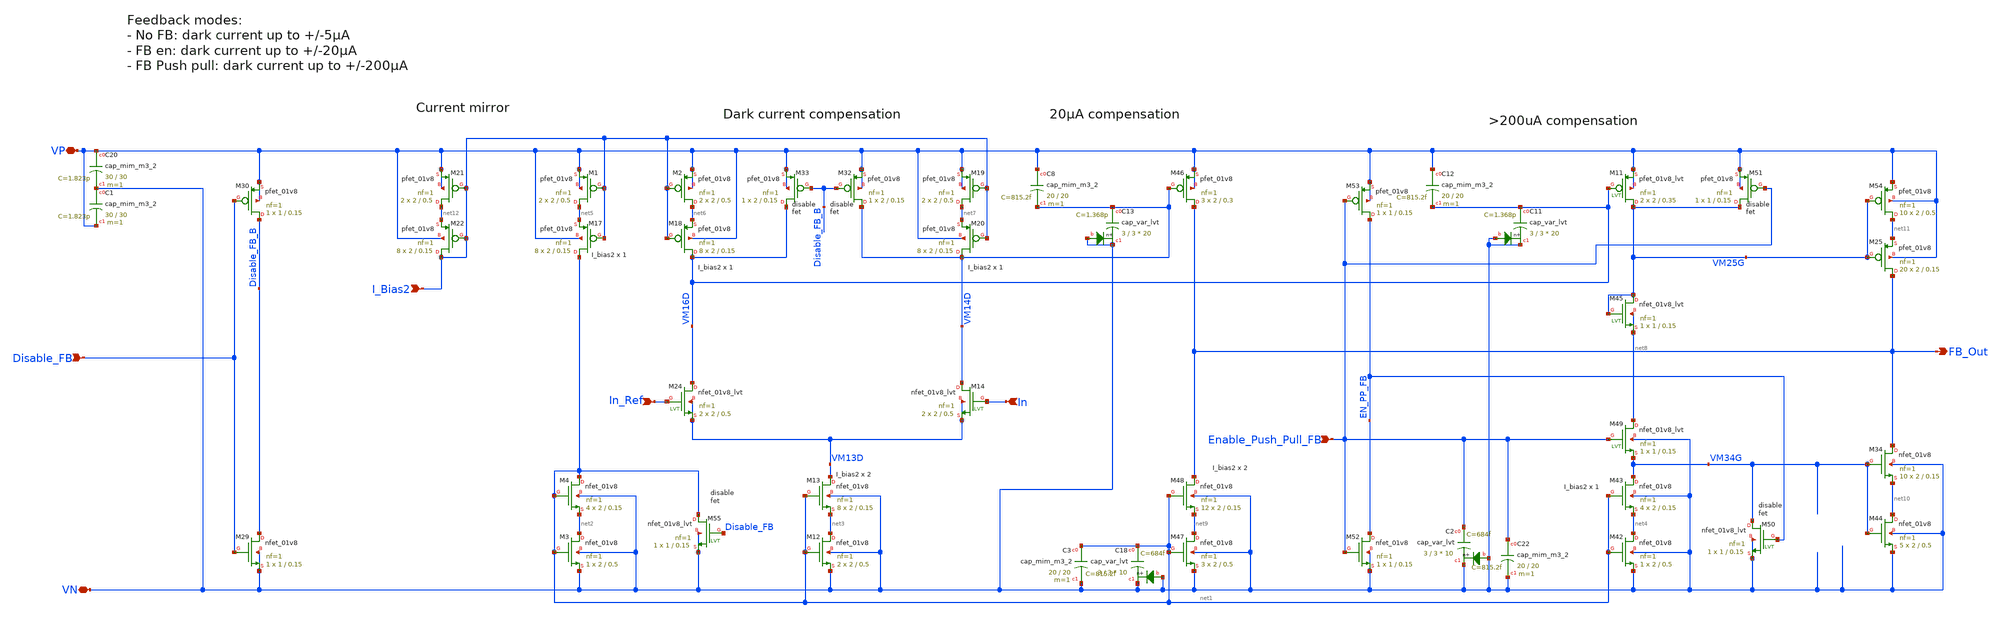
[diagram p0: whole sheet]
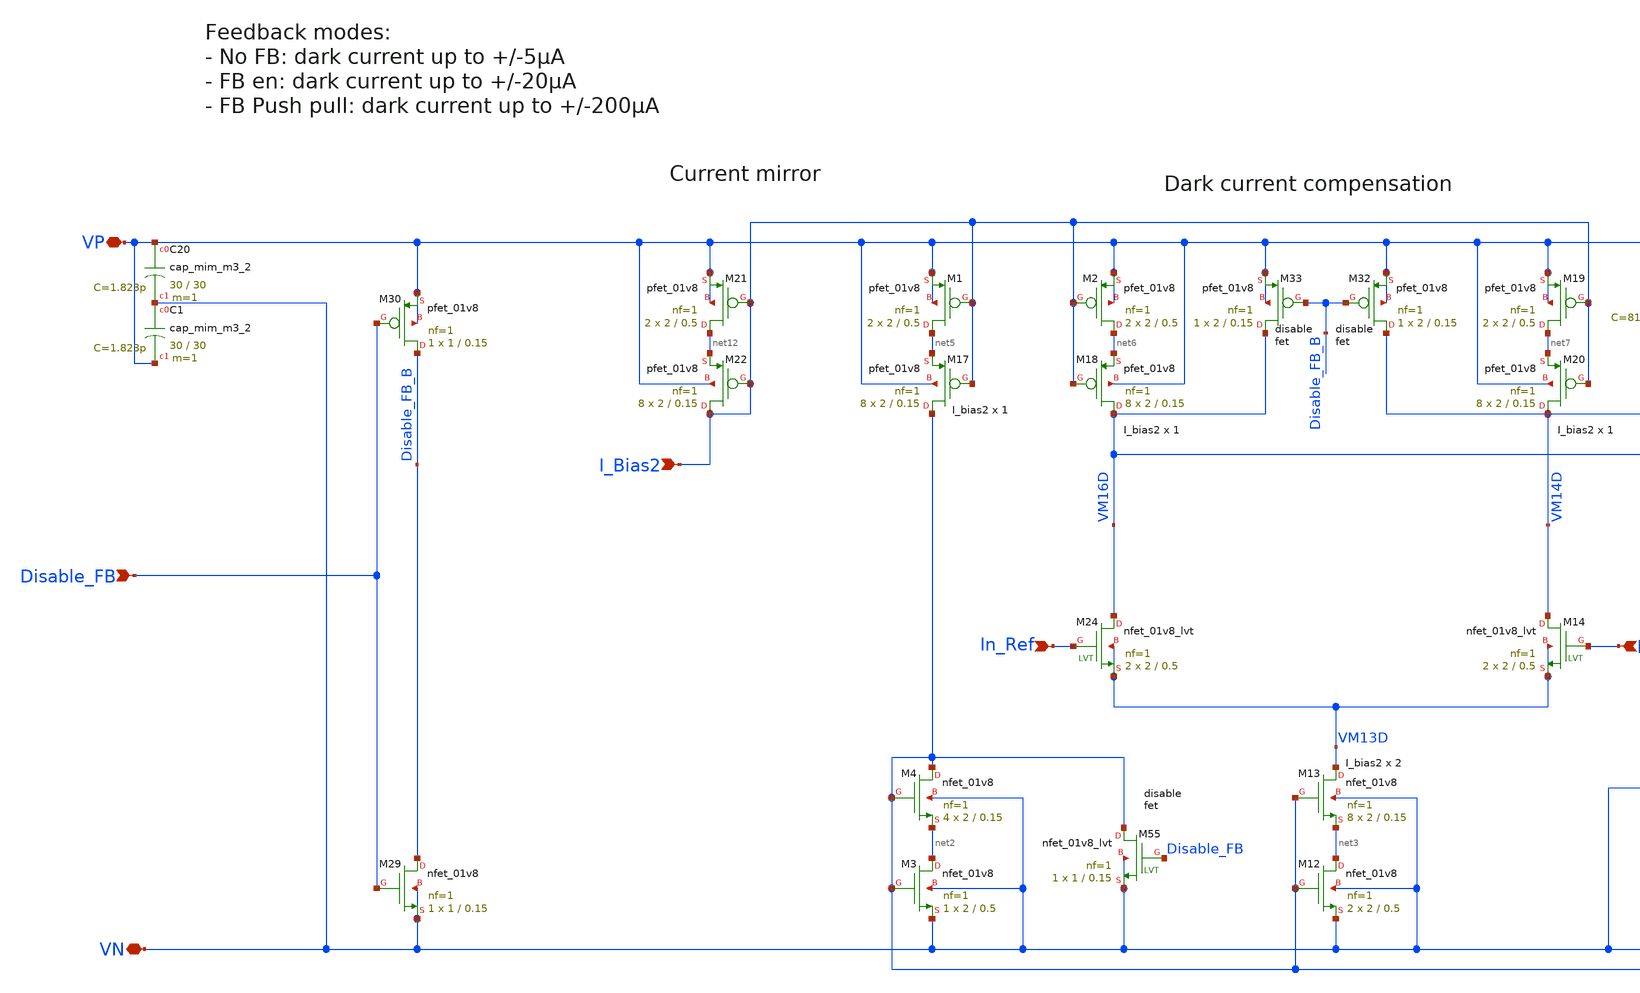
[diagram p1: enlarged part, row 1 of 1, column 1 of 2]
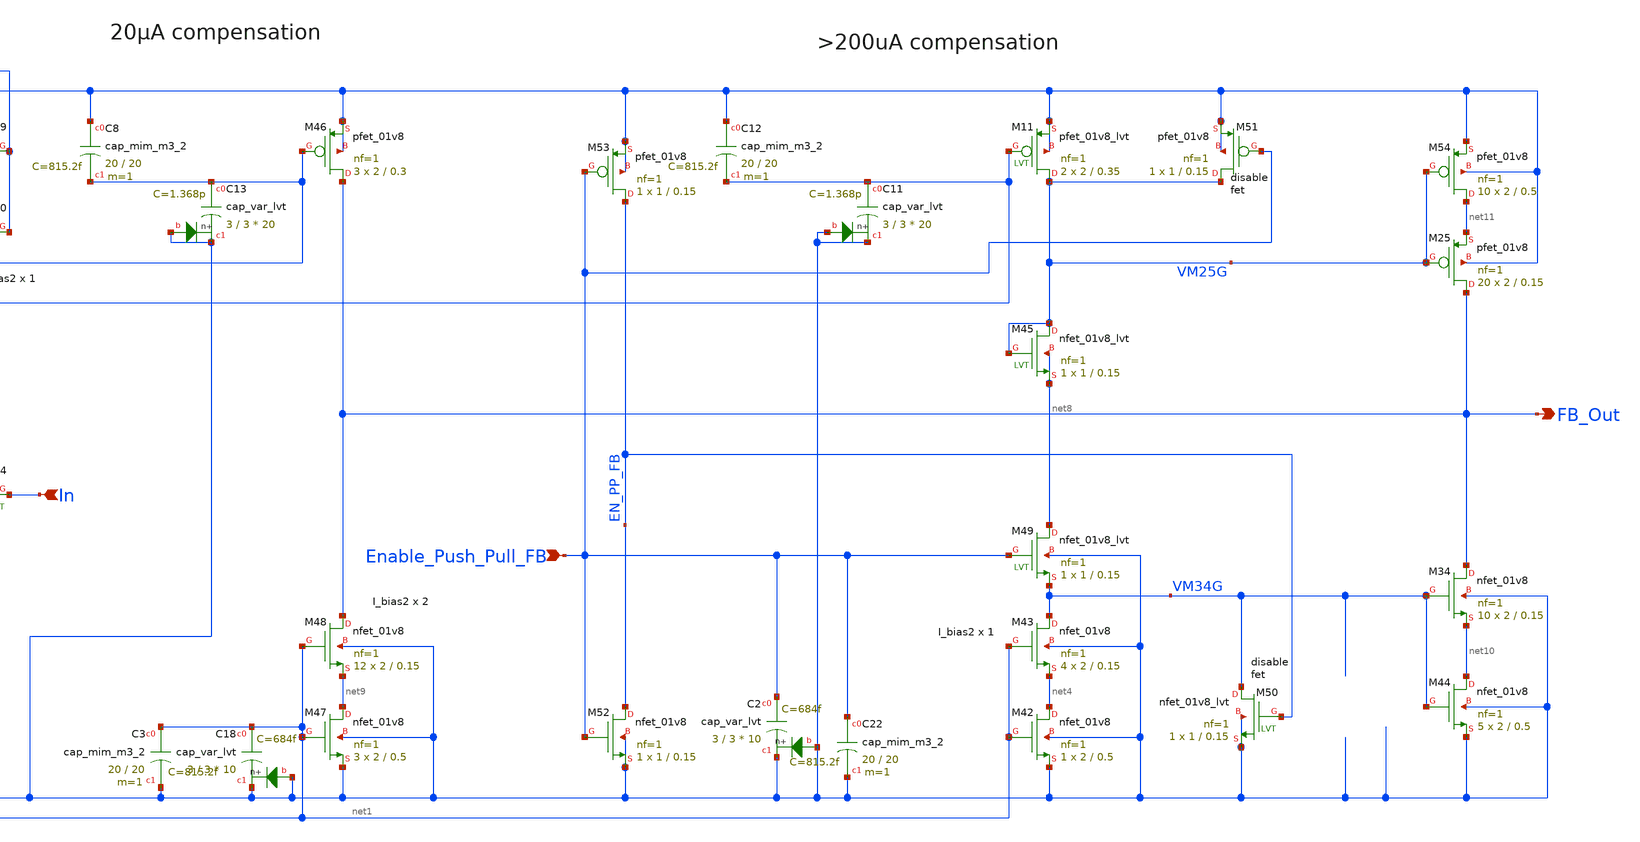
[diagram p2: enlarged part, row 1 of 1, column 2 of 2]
** sch_path: xschem/tia/tia_rgc_feedback.sch
**.subckt tia_rgc_feedback VN VP I_Bias2 Disable_FB Enable_Push_Pull_FB In_Ref FB_Out In
*.iopin VN
*.iopin VP
*.ipin I_Bias2
*.ipin Disable_FB
*.ipin Enable_Push_Pull_FB
*.ipin In_Ref
*.opin FB_Out
*.ipin In
XM3 net2 net1 VN VN sky130_fd_pr__nfet_01v8 L=0.5 W=2 nf=1 ad='int((nf+1)/2) * W/nf * 0.29' as='int((nf+2)/2) * W/nf * 0.29'
+ pd='2*int((nf+1)/2) * (W/nf + 0.29)' ps='2*int((nf+2)/2) * (W/nf + 0.29)' nrd='0.29 / W' nrs='0.29 / W'
+ sa=0 sb=0 sd=0 mult=1 m=1
XM4 net1 net1 net2 VN sky130_fd_pr__nfet_01v8 L=0.15 W=2 nf=1 ad='int((nf+1)/2) * W/nf * 0.29' as='int((nf+2)/2) * W/nf * 0.29'
+ pd='2*int((nf+1)/2) * (W/nf + 0.29)' ps='2*int((nf+2)/2) * (W/nf + 0.29)' nrd='0.29 / W' nrs='0.29 / W'
+ sa=0 sb=0 sd=0 mult=4 m=4
XM12 net3 net1 VN VN sky130_fd_pr__nfet_01v8 L=0.5 W=2 nf=1 ad='int((nf+1)/2) * W/nf * 0.29' as='int((nf+2)/2) * W/nf * 0.29'
+ pd='2*int((nf+1)/2) * (W/nf + 0.29)' ps='2*int((nf+2)/2) * (W/nf + 0.29)' nrd='0.29 / W' nrs='0.29 / W'
+ sa=0 sb=0 sd=0 mult=2 m=2
XM13 VM13D net1 net3 VN sky130_fd_pr__nfet_01v8 L=0.15 W=2 nf=1 ad='int((nf+1)/2) * W/nf * 0.29' as='int((nf+2)/2) * W/nf * 0.29'
+ pd='2*int((nf+1)/2) * (W/nf + 0.29)' ps='2*int((nf+2)/2) * (W/nf + 0.29)' nrd='0.29 / W' nrs='0.29 / W'
+ sa=0 sb=0 sd=0 mult=8 m=8
XM1 net5 I_Bias2 VP VP sky130_fd_pr__pfet_01v8 L=0.5 W=2 nf=1 ad='int((nf+1)/2) * W/nf * 0.29' as='int((nf+2)/2) * W/nf * 0.29'
+ pd='2*int((nf+1)/2) * (W/nf + 0.29)' ps='2*int((nf+2)/2) * (W/nf + 0.29)' nrd='0.29 / W' nrs='0.29 / W'
+ sa=0 sb=0 sd=0 mult=2 m=2
XM29 Disable_FB_B Disable_FB VN VN sky130_fd_pr__nfet_01v8 L=0.15 W=1 nf=1 ad='int((nf+1)/2) * W/nf * 0.29'
+ as='int((nf+2)/2) * W/nf * 0.29' pd='2*int((nf+1)/2) * (W/nf + 0.29)' ps='2*int((nf+2)/2) * (W/nf + 0.29)'
+ nrd='0.29 / W' nrs='0.29 / W' sa=0 sb=0 sd=0 mult=1 m=1
XM30 Disable_FB_B Disable_FB VP VP sky130_fd_pr__pfet_01v8 L=0.15 W=1 nf=1 ad='int((nf+1)/2) * W/nf * 0.29'
+ as='int((nf+2)/2) * W/nf * 0.29' pd='2*int((nf+1)/2) * (W/nf + 0.29)' ps='2*int((nf+2)/2) * (W/nf + 0.29)'
+ nrd='0.29 / W' nrs='0.29 / W' sa=0 sb=0 sd=0 mult=1 m=1
XM32 VM14D Disable_FB_B VP VP sky130_fd_pr__pfet_01v8 L=0.15 W=2 nf=1 ad='int((nf+1)/2) * W/nf * 0.29'
+ as='int((nf+2)/2) * W/nf * 0.29' pd='2*int((nf+1)/2) * (W/nf + 0.29)' ps='2*int((nf+2)/2) * (W/nf + 0.29)'
+ nrd='0.29 / W' nrs='0.29 / W' sa=0 sb=0 sd=0 mult=1 m=1
XM33 VM16D Disable_FB_B VP VP sky130_fd_pr__pfet_01v8 L=0.15 W=2 nf=1 ad='int((nf+1)/2) * W/nf * 0.29'
+ as='int((nf+2)/2) * W/nf * 0.29' pd='2*int((nf+1)/2) * (W/nf + 0.29)' ps='2*int((nf+2)/2) * (W/nf + 0.29)'
+ nrd='0.29 / W' nrs='0.29 / W' sa=0 sb=0 sd=0 mult=1 m=1
XM42 net4 net1 VN VN sky130_fd_pr__nfet_01v8 L=0.5 W=2 nf=1 ad='int((nf+1)/2) * W/nf * 0.29' as='int((nf+2)/2) * W/nf * 0.29'
+ pd='2*int((nf+1)/2) * (W/nf + 0.29)' ps='2*int((nf+2)/2) * (W/nf + 0.29)' nrd='0.29 / W' nrs='0.29 / W'
+ sa=0 sb=0 sd=0 mult=1 m=1
XM43 VM34G net1 net4 VN sky130_fd_pr__nfet_01v8 L=0.15 W=2 nf=1 ad='int((nf+1)/2) * W/nf * 0.29' as='int((nf+2)/2) * W/nf * 0.29'
+ pd='2*int((nf+1)/2) * (W/nf + 0.29)' ps='2*int((nf+2)/2) * (W/nf + 0.29)' nrd='0.29 / W' nrs='0.29 / W'
+ sa=0 sb=0 sd=0 mult=4 m=4
XM17 net1 I_Bias2 net5 VP sky130_fd_pr__pfet_01v8 L=0.15 W=2 nf=1 ad='int((nf+1)/2) * W/nf * 0.29' as='int((nf+2)/2) * W/nf * 0.29'
+ pd='2*int((nf+1)/2) * (W/nf + 0.29)' ps='2*int((nf+2)/2) * (W/nf + 0.29)' nrd='0.29 / W' nrs='0.29 / W'
+ sa=0 sb=0 sd=0 mult=8 m=8
XM2 net6 I_Bias2 VP VP sky130_fd_pr__pfet_01v8 L=0.5 W=2 nf=1 ad='int((nf+1)/2) * W/nf * 0.29' as='int((nf+2)/2) * W/nf * 0.29'
+ pd='2*int((nf+1)/2) * (W/nf + 0.29)' ps='2*int((nf+2)/2) * (W/nf + 0.29)' nrd='0.29 / W' nrs='0.29 / W'
+ sa=0 sb=0 sd=0 mult=2 m=2
XM18 VM16D I_Bias2 net6 VP sky130_fd_pr__pfet_01v8 L=0.15 W=2 nf=1 ad='int((nf+1)/2) * W/nf * 0.29' as='int((nf+2)/2) * W/nf * 0.29'
+ pd='2*int((nf+1)/2) * (W/nf + 0.29)' ps='2*int((nf+2)/2) * (W/nf + 0.29)' nrd='0.29 / W' nrs='0.29 / W'
+ sa=0 sb=0 sd=0 mult=8 m=8
XM19 net7 I_Bias2 VP VP sky130_fd_pr__pfet_01v8 L=0.5 W=2 nf=1 ad='int((nf+1)/2) * W/nf * 0.29' as='int((nf+2)/2) * W/nf * 0.29'
+ pd='2*int((nf+1)/2) * (W/nf + 0.29)' ps='2*int((nf+2)/2) * (W/nf + 0.29)' nrd='0.29 / W' nrs='0.29 / W'
+ sa=0 sb=0 sd=0 mult=2 m=2
XM20 VM14D I_Bias2 net7 VP sky130_fd_pr__pfet_01v8 L=0.15 W=2 nf=1 ad='int((nf+1)/2) * W/nf * 0.29' as='int((nf+2)/2) * W/nf * 0.29'
+ pd='2*int((nf+1)/2) * (W/nf + 0.29)' ps='2*int((nf+2)/2) * (W/nf + 0.29)' nrd='0.29 / W' nrs='0.29 / W'
+ sa=0 sb=0 sd=0 mult=8 m=8
XM34 FB_Out VM34G net10 VN sky130_fd_pr__nfet_01v8 L=0.15 W=2 nf=1 ad='int((nf+1)/2) * W/nf * 0.29' as='int((nf+2)/2) * W/nf * 0.29'
+ pd='2*int((nf+1)/2) * (W/nf + 0.29)' ps='2*int((nf+2)/2) * (W/nf + 0.29)' nrd='0.29 / W' nrs='0.29 / W'
+ sa=0 sb=0 sd=0 mult=10 m=10
XM25 FB_Out VM25G net11 VP sky130_fd_pr__pfet_01v8 L=0.15 W=2 nf=1 ad='int((nf+1)/2) * W/nf * 0.29' as='int((nf+2)/2) * W/nf * 0.29'
+ pd='2*int((nf+1)/2) * (W/nf + 0.29)' ps='2*int((nf+2)/2) * (W/nf + 0.29)' nrd='0.29 / W' nrs='0.29 / W'
+ sa=0 sb=0 sd=0 mult=20 m=20
XM45 VM25G VM25G net8 net8 sky130_fd_pr__nfet_01v8_lvt L=0.15 W=1 nf=1 ad='int((nf+1)/2) * W/nf * 0.29'
+ as='int((nf+2)/2) * W/nf * 0.29' pd='2*int((nf+1)/2) * (W/nf + 0.29)' ps='2*int((nf+2)/2) * (W/nf + 0.29)'
+ nrd='0.29 / W' nrs='0.29 / W' sa=0 sb=0 sd=0 mult=1 m=1
XM46 FB_Out VM14D VP VP sky130_fd_pr__pfet_01v8 L=0.3 W=2 nf=1 ad='int((nf+1)/2) * W/nf * 0.29' as='int((nf+2)/2) * W/nf * 0.29'
+ pd='2*int((nf+1)/2) * (W/nf + 0.29)' ps='2*int((nf+2)/2) * (W/nf + 0.29)' nrd='0.29 / W' nrs='0.29 / W'
+ sa=0 sb=0 sd=0 mult=3 m=3
XM47 net9 net1 VN VN sky130_fd_pr__nfet_01v8 L=0.5 W=2 nf=1 ad='int((nf+1)/2) * W/nf * 0.29' as='int((nf+2)/2) * W/nf * 0.29'
+ pd='2*int((nf+1)/2) * (W/nf + 0.29)' ps='2*int((nf+2)/2) * (W/nf + 0.29)' nrd='0.29 / W' nrs='0.29 / W'
+ sa=0 sb=0 sd=0 mult=3 m=3
XM48 FB_Out net1 net9 VN sky130_fd_pr__nfet_01v8 L=0.15 W=2 nf=1 ad='int((nf+1)/2) * W/nf * 0.29' as='int((nf+2)/2) * W/nf * 0.29'
+ pd='2*int((nf+1)/2) * (W/nf + 0.29)' ps='2*int((nf+2)/2) * (W/nf + 0.29)' nrd='0.29 / W' nrs='0.29 / W'
+ sa=0 sb=0 sd=0 mult=12 m=12
XC8 VP VM14D sky130_fd_pr__cap_mim_m3_2 W=20 L=20 MF=1 m=1
XM52 EN_PP_FB Enable_Push_Pull_FB VN VN sky130_fd_pr__nfet_01v8 L=0.15 W=1 nf=1 ad='int((nf+1)/2) * W/nf * 0.29'
+ as='int((nf+2)/2) * W/nf * 0.29' pd='2*int((nf+1)/2) * (W/nf + 0.29)' ps='2*int((nf+2)/2) * (W/nf + 0.29)'
+ nrd='0.29 / W' nrs='0.29 / W' sa=0 sb=0 sd=0 mult=1 m=1
XM53 EN_PP_FB Enable_Push_Pull_FB VP VP sky130_fd_pr__pfet_01v8 L=0.15 W=1 nf=1 ad='int((nf+1)/2) * W/nf * 0.29'
+ as='int((nf+2)/2) * W/nf * 0.29' pd='2*int((nf+1)/2) * (W/nf + 0.29)' ps='2*int((nf+2)/2) * (W/nf + 0.29)'
+ nrd='0.29 / W' nrs='0.29 / W' sa=0 sb=0 sd=0 mult=1 m=1
XM49 net8 Enable_Push_Pull_FB VM34G VN sky130_fd_pr__nfet_01v8_lvt L=0.15 W=1 nf=1 ad='int((nf+1)/2) * W/nf * 0.29'
+ as='int((nf+2)/2) * W/nf * 0.29' pd='2*int((nf+1)/2) * (W/nf + 0.29)' ps='2*int((nf+2)/2) * (W/nf + 0.29)'
+ nrd='0.29 / W' nrs='0.29 / W' sa=0 sb=0 sd=0 mult=1 m=1
XM50 VM34G EN_PP_FB VN VN sky130_fd_pr__nfet_01v8_lvt L=0.15 W=1 nf=1 ad='int((nf+1)/2) * W/nf * 0.29'
+ as='int((nf+2)/2) * W/nf * 0.29' pd='2*int((nf+1)/2) * (W/nf + 0.29)' ps='2*int((nf+2)/2) * (W/nf + 0.29)'
+ nrd='0.29 / W' nrs='0.29 / W' sa=0 sb=0 sd=0 mult=1 m=1
XM51 VM25G Enable_Push_Pull_FB VP VP sky130_fd_pr__pfet_01v8 L=0.15 W=1 nf=1 ad='int((nf+1)/2) * W/nf * 0.29'
+ as='int((nf+2)/2) * W/nf * 0.29' pd='2*int((nf+1)/2) * (W/nf + 0.29)' ps='2*int((nf+2)/2) * (W/nf + 0.29)'
+ nrd='0.29 / W' nrs='0.29 / W' sa=0 sb=0 sd=0 mult=1 m=1
XM44 net10 VM34G VN VN sky130_fd_pr__nfet_01v8 L=0.5 W=2 nf=1 ad='int((nf+1)/2) * W/nf * 0.29' as='int((nf+2)/2) * W/nf * 0.29'
+ pd='2*int((nf+1)/2) * (W/nf + 0.29)' ps='2*int((nf+2)/2) * (W/nf + 0.29)' nrd='0.29 / W' nrs='0.29 / W'
+ sa=0 sb=0 sd=0 mult=5 m=5
XM54 net11 VM25G VP VP sky130_fd_pr__pfet_01v8 L=0.5 W=2 nf=1 ad='int((nf+1)/2) * W/nf * 0.29' as='int((nf+2)/2) * W/nf * 0.29'
+ pd='2*int((nf+1)/2) * (W/nf + 0.29)' ps='2*int((nf+2)/2) * (W/nf + 0.29)' nrd='0.29 / W' nrs='0.29 / W'
+ sa=0 sb=0 sd=0 mult=10 m=10
XM11 VM25G VM16D VP VP sky130_fd_pr__pfet_01v8_lvt L=0.35 W=2 nf=1 ad='int((nf+1)/2) * W/nf * 0.29' as='int((nf+2)/2) * W/nf * 0.29'
+ pd='2*int((nf+1)/2) * (W/nf + 0.29)' ps='2*int((nf+2)/2) * (W/nf + 0.29)' nrd='0.29 / W' nrs='0.29 / W'
+ sa=0 sb=0 sd=0 mult=2 m=2
XC20 VP VN sky130_fd_pr__cap_mim_m3_2 W=30 L=30 MF=1 m=1
XC18 net1 VN VN sky130_fd_pr__cap_var_lvt W=3 L=3 VM=10 m=10
XC11 VM16D VN VN sky130_fd_pr__cap_var_lvt W=3 L=3 VM=20 m=20
XC12 VP VM16D sky130_fd_pr__cap_mim_m3_2 W=20 L=20 MF=1 m=1
XC22 Enable_Push_Pull_FB VN sky130_fd_pr__cap_mim_m3_2 W=20 L=20 MF=1 m=1
XM21 net12 I_Bias2 VP VP sky130_fd_pr__pfet_01v8 L=0.5 W=2 nf=1 ad='int((nf+1)/2) * W/nf * 0.29' as='int((nf+2)/2) * W/nf * 0.29'
+ pd='2*int((nf+1)/2) * (W/nf + 0.29)' ps='2*int((nf+2)/2) * (W/nf + 0.29)' nrd='0.29 / W' nrs='0.29 / W'
+ sa=0 sb=0 sd=0 mult=2 m=2
XM22 I_Bias2 I_Bias2 net12 VP sky130_fd_pr__pfet_01v8 L=0.15 W=2 nf=1 ad='int((nf+1)/2) * W/nf * 0.29'
+ as='int((nf+2)/2) * W/nf * 0.29' pd='2*int((nf+1)/2) * (W/nf + 0.29)' ps='2*int((nf+2)/2) * (W/nf + 0.29)'
+ nrd='0.29 / W' nrs='0.29 / W' sa=0 sb=0 sd=0 mult=8 m=8
XM55 net1 Disable_FB VN VN sky130_fd_pr__nfet_01v8_lvt L=0.15 W=1 nf=1 ad='int((nf+1)/2) * W/nf * 0.29'
+ as='int((nf+2)/2) * W/nf * 0.29' pd='2*int((nf+1)/2) * (W/nf + 0.29)' ps='2*int((nf+2)/2) * (W/nf + 0.29)'
+ nrd='0.29 / W' nrs='0.29 / W' sa=0 sb=0 sd=0 mult=1 m=1
XM24 VM16D In_Ref VM13D VM13D sky130_fd_pr__nfet_01v8_lvt L=0.5 W=2 nf=1 ad='int((nf+1)/2) * W/nf * 0.29'
+ as='int((nf+2)/2) * W/nf * 0.29' pd='2*int((nf+1)/2) * (W/nf + 0.29)' ps='2*int((nf+2)/2) * (W/nf + 0.29)'
+ nrd='0.29 / W' nrs='0.29 / W' sa=0 sb=0 sd=0 mult=2 m=2
XM14 VM14D In VM13D VM13D sky130_fd_pr__nfet_01v8_lvt L=0.5 W=2 nf=1 ad='int((nf+1)/2) * W/nf * 0.29'
+ as='int((nf+2)/2) * W/nf * 0.29' pd='2*int((nf+1)/2) * (W/nf + 0.29)' ps='2*int((nf+2)/2) * (W/nf + 0.29)'
+ nrd='0.29 / W' nrs='0.29 / W' sa=0 sb=0 sd=0 mult=2 m=2
XC13 VM14D VN VN sky130_fd_pr__cap_var_lvt W=3 L=3 VM=20 m=20
XC1 VN VP sky130_fd_pr__cap_mim_m3_2 W=30 L=30 MF=1 m=1
XC2 Enable_Push_Pull_FB VN VN sky130_fd_pr__cap_var_lvt W=3 L=3 VM=10 m=10
XC3 net1 VN sky130_fd_pr__cap_mim_m3_2 W=20 L=20 MF=1 m=1
**.ends
.end
